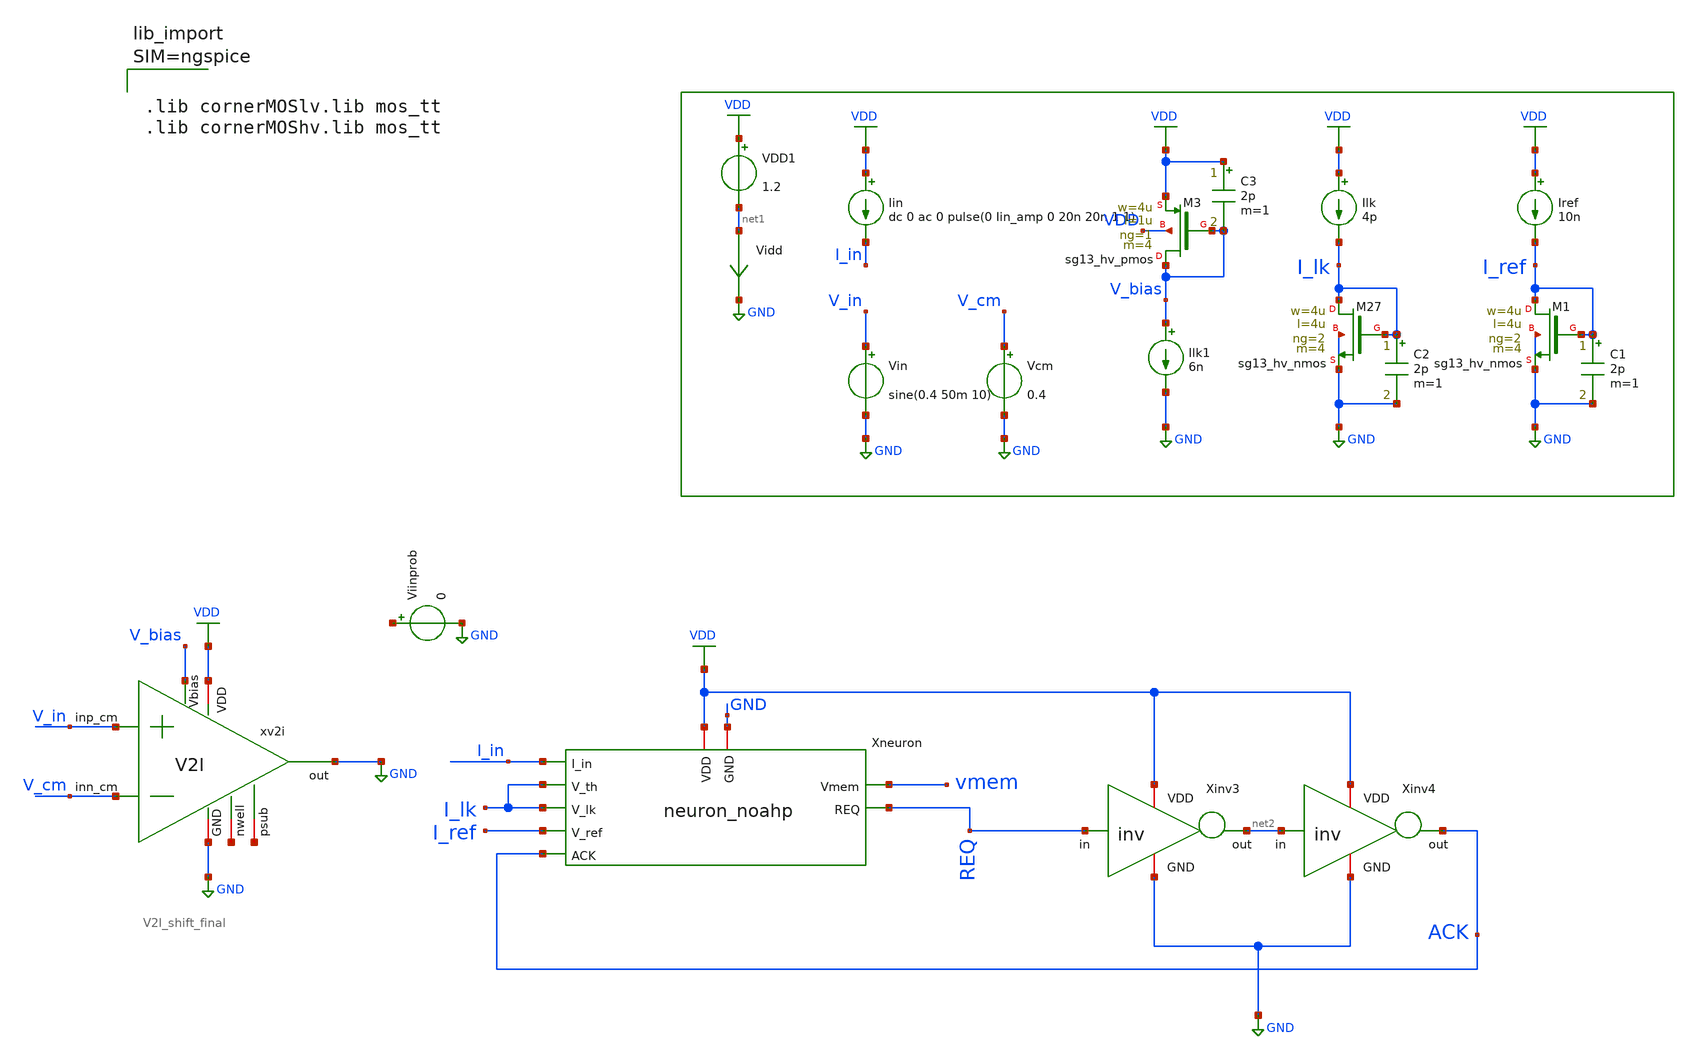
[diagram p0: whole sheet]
** sch_path: xschem/neuron_noahp_tb.sch
**.subckt neuron_noahp_tb
Xneuron VDD I_in I_lk I_lk vmem REQ ACK I_ref GND neuron_noahp
Ilk VDD I_lk 4p
Iin VDD I_in dc 0 ac 0 pulse(0 Iin_amp 0 20n 20n 1 1)
VDD1 VDD net1 1.2
Iref VDD I_ref 10n
Vidd net1 GND 0
.save i(vidd)
XM27 I_lk I_lk GND GND sg13_hv_nmos w=4u l=4u ng=2 m=4 mm_ok=1
Xinv3 VDD REQ net2 GND inv
Xinv4 VDD net2 ACK GND inv
C2 I_lk GND 2p m=1
XM1 I_ref I_ref GND GND sg13_hv_nmos w=4u l=4u ng=2 m=4 mm_ok=1
C1 I_ref GND 2p m=1
xv2i VDD V_bias V_cm V_in GND GND net3 net4 V2I_shift_final
XM3 V_bias V_bias VDD VDD sg13_hv_pmos w=4u l=1u ng=1 m=4 mm_ok=1
C3 VDD V_bias 2p m=1
Ilk1 V_bias GND 6n
Vcm V_cm GND 0.4
Vin V_in GND sine(0.4 50m 10)
Viinprob net5 GND 0
.save i(viinprob)
**** begin user architecture code



.param temp=27
.param Iin_amp=200p

.ic V(vmem)=0 V(xneuron.xref.vref)=0 V(REQ)=1.2 V(ACK)=1.2

.options gmin=1e-13
.options method=gear
.control



* ======================================================
*  Iin sweep - measure firing rate of V(REQ) vs Iin
* ======================================================
*  For each DC value of Iin a transient simulation is run.
*  Rising-edge crossings of V(REQ) through a threshold
*  are counted after a settling window and the firing
*  frequency is computed.  Results go to neuron_iin_sweep.raw
* ======================================================

* --- Sweep parameters (Amps) - edit as needed ---
let iin_start = 0
let iin_stop  = 4000e-12
let iin_step  = 200e-12

* --- Compute number of sweep points ---
let num_pts = (iin_stop - iin_start) / iin_step + 1

* --- Create a new plot to hold the accumulated results ---
setplot new
set resplot = $curplot
let iin_values   = unitvec(num_pts)
let firing_rates = unitvec(num_pts)
let sweep_idx = 0
set t_sim = 50m

* --- Main sweep loop ---
dowhile sweep_idx < num_pts

  * Compute cur_iin fresh each iteration to avoid float drift
  let cur_iin = iin_start + sweep_idx * iin_step

  echo
  echo ============================================
  echo   Sweep point: Iin = $&cur_iin A
  echo ============================================

  * Save cur_iin to a shell variable before tran changes the plot context
  set cur_iin_val = $&cur_iin

  * Set the Iin_amp parameter to the current sweep value.
  alterparam Iin_amp = $cur_iin_val
  reset

  save V(REQ)

  * Run transient analysis with adaptive time
  echo   t_sim = $t_sim
  tran 50n $t_sim

  * --- Measure firing frequency using meas tran ---
  * Skip 1st spike (different freq from resting), use 2nd-4th spikes
  let t_fall1 = 0
  let t_fall2 = 0
  let t_fall3 = 0
  let t_fall4 = 0
  meas tran t_fall1 WHEN v(REQ)=0.6 FALL=1
  meas tran t_fall2 WHEN v(REQ)=0.6 FALL=2
  meas tran t_fall3 WHEN v(REQ)=0.6 FALL=3
  meas tran t_fall4 WHEN v(REQ)=0.6 FALL=4

  * Use best available data for frequency
  * More than 1 spike: f = (N-1) / (t_last - t_first)
  * Exactly 1 spike:   f = 1 / t_first
  if t_fall4 > 0
    * 4 spikes: use span from 1st to 4th
    let f_rate = 3.0 / (t_fall4 - t_fall1)
  else
    if t_fall3 > 0
      * 3 spikes: use span from 1st to 3rd
      let f_rate = 2.0 / (t_fall3 - t_fall1)
    else
      if t_fall2 > 0
        * 2 spikes: use span from 1st to 2nd
        let f_rate = 1.0 / (t_fall2 - t_fall1)
      else
        if t_fall1 > 0
          * 1 spike: estimate from time to 1st spike
          let f_rate = 1.0 / t_fall1
        else
          * No spikes
          let f_rate = 0
        end
      end
    end
  end

  echo   freq = $&f_rate Hz
  echo   Spike times:
  echo     t_fall1 = $&t_fall1 s
  echo     t_fall2 = $&t_fall2 s
  echo     t_fall3 = $&t_fall3 s
  echo     t_fall4 = $&t_fall4 s

  * --- Update t_sim for next sweep point ---
  * Need ~5 spikes worth of time, clamp to [1ms, 50ms]
  if f_rate > 0
    let t_next = 5.0 / f_rate
    if t_next < 1e-3
      let t_next = 1e-3
    end
    if t_next > 50e-3
      let t_next = 50e-3
    end
    set t_sim = $&t_next
  end

  * --- Store this point's results in the result plot ---
  set save_freq = $&f_rate
  setplot $resplot
  let iin_values[sweep_idx]   = $cur_iin_val
  let firing_rates[sweep_idx] = $save_freq
  let sweep_idx = sweep_idx + 1

end

* --- Write the result vectors to a .raw file ---
setplot $resplot
write neuron_iin_sweep.raw iin_values firing_rates

echo
echo ============================================
echo   Iin sweep complete!
echo   Results saved to:  neuron_iin_sweep.raw
echo   Vectors:
echo     iin_values   (A)  - input current
echo     firing_rates (Hz) - neuron firing rate
echo ============================================

.endc







.lib cornerMOSlv.lib mos_tt
.lib cornerMOShv.lib mos_tt


**** end user architecture code
**.ends
.GLOBAL GND
.GLOBAL VDD
.end
